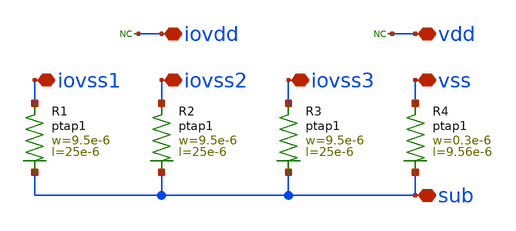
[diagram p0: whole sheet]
** sch_path: MSPHY6034-main/schematic/xschem/openpdk-libraries/ihp-sg13g2/sg13g2_io/xschem/sg13g2_Filler2000.sch
**.subckt sg13g2_Filler2000 iovss1 iovss2 iovss3 vss iovdd vdd sub
*.iopin iovss1
*.iopin iovss2
*.iopin iovss3
*.iopin vss
*.iopin iovdd
*.iopin vdd
*.iopin sub
XR3 iovss3 sub ptap1 R=3.197 w=9.5e-6 l=25e-6
XR4 vss sub ptap1 R=43.39 w=0.3e-6 l=9.56e-6
* noconn iovdd
* noconn vdd
XR1 iovss1 sub ptap1 R=3.197 w=9.5e-6 l=25e-6
XR2 iovss2 sub ptap1 R=3.197 w=9.5e-6 l=25e-6
**.ends
.end
